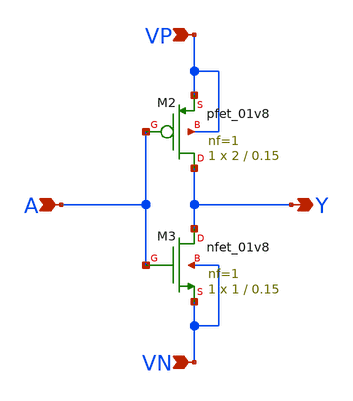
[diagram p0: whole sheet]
** sch_path: VLSI/P_D_S_TEST_05/VLSI_TEST_05 (Post_Design_Simulation))/inv_R1.sch
**.subckt inv_R1 A Y VP VN
*.ipin A
*.opin Y
*.ipin VP
*.ipin VN
XM2 Y A VP VP sky130_fd_pr__pfet_01v8 L=0.15 W=2 nf=1 ad='int((nf+1)/2) * W/nf * 0.29' as='int((nf+2)/2) * W/nf * 0.29'
+ pd='2*int((nf+1)/2) * (W/nf + 0.29)' ps='2*int((nf+2)/2) * (W/nf + 0.29)' nrd='0.29 / W' nrs='0.29 / W'
+ sa=0 sb=0 sd=0 mult=1 m=1
XM3 Y A VN VN sky130_fd_pr__nfet_01v8 L=0.15 W=1 nf=1 ad='int((nf+1)/2) * W/nf * 0.29' as='int((nf+2)/2) * W/nf * 0.29'
+ pd='2*int((nf+1)/2) * (W/nf + 0.29)' ps='2*int((nf+2)/2) * (W/nf + 0.29)' nrd='0.29 / W' nrs='0.29 / W'
+ sa=0 sb=0 sd=0 mult=1 m=1
**.ends
.end
